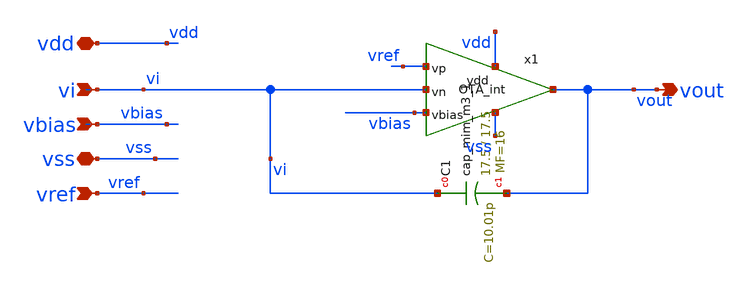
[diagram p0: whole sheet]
** sch_path: xschem/src/integrator/integrator.sch
**.subckt integrator vi vbias vss vdd vout vref
*.ipin vi
*.ipin vbias
*.iopin vss
*.iopin vdd
*.opin vout
*.ipin vref
x1 vdd vref vi vbias vss vout OTA_int
XC1 vi vout sky130_fd_pr__cap_mim_m3_1 W=17.5 L=17.5 MF=16 m=16
**.ends

* expanding   symbol:  src/OTA_int/OTA_int.sym # of pins=6
** sym_path: xschem/src/OTA_int/OTA_int.sym
** sch_path: xschem/src/OTA_int/OTA_int.sch
.subckt OTA_int vdd vp vn vbias vss vout
*.ipin vp
*.ipin vn
*.ipin vbias
*.iopin vss
*.iopin vdd
*.opin vout
XM1 v1 vp vc vc sky130_fd_pr__pfet_01v8_lvt L=1 W=4 nf=1 ad='int((nf+1)/2) * W/nf * 0.29' as='int((nf+2)/2) * W/nf * 0.29'
+ pd='2*int((nf+1)/2) * (W/nf + 0.29)' ps='2*int((nf+2)/2) * (W/nf + 0.29)' nrd='0.29 / W' nrs='0.29 / W'
+ sa=0 sb=0 sd=0 mult=16 m=16
XM2 vf vn vc vc sky130_fd_pr__pfet_01v8_lvt L=1 W=4 nf=1 ad='int((nf+1)/2) * W/nf * 0.29' as='int((nf+2)/2) * W/nf * 0.29'
+ pd='2*int((nf+1)/2) * (W/nf + 0.29)' ps='2*int((nf+2)/2) * (W/nf + 0.29)' nrd='0.29 / W' nrs='0.29 / W'
+ sa=0 sb=0 sd=0 mult=16 m=16
XM3 vc vbias vdd vdd sky130_fd_pr__pfet_01v8_lvt L=1 W=2 nf=2 ad='int((nf+1)/2) * W/nf * 0.29' as='int((nf+2)/2) * W/nf * 0.29'
+ pd='2*int((nf+1)/2) * (W/nf + 0.29)' ps='2*int((nf+2)/2) * (W/nf + 0.29)' nrd='0.29 / W' nrs='0.29 / W'
+ sa=0 sb=0 sd=0 mult=24 m=24
XM4 v1 vf vss vss sky130_fd_pr__nfet_01v8_lvt L=1 W=1 nf=1 ad='int((nf+1)/2) * W/nf * 0.29' as='int((nf+2)/2) * W/nf * 0.29'
+ pd='2*int((nf+1)/2) * (W/nf + 0.29)' ps='2*int((nf+2)/2) * (W/nf + 0.29)' nrd='0.29 / W' nrs='0.29 / W'
+ sa=0 sb=0 sd=0 mult=16 m=16
XM5 vf vf vss vss sky130_fd_pr__nfet_01v8_lvt L=1 W=1 nf=1 ad='int((nf+1)/2) * W/nf * 0.29' as='int((nf+2)/2) * W/nf * 0.29'
+ pd='2*int((nf+1)/2) * (W/nf + 0.29)' ps='2*int((nf+2)/2) * (W/nf + 0.29)' nrd='0.29 / W' nrs='0.29 / W'
+ sa=0 sb=0 sd=0 mult=16 m=16
XM6 vbias vbias vdd vdd sky130_fd_pr__pfet_01v8_lvt L=1 W=2 nf=2 ad='int((nf+1)/2) * W/nf * 0.29' as='int((nf+2)/2) * W/nf * 0.29'
+ pd='2*int((nf+1)/2) * (W/nf + 0.29)' ps='2*int((nf+2)/2) * (W/nf + 0.29)' nrd='0.29 / W' nrs='0.29 / W'
+ sa=0 sb=0 sd=0 mult=24 m=24
XM7 vout vbias vdd vdd sky130_fd_pr__pfet_01v8_lvt L=1 W=2 nf=2 ad='int((nf+1)/2) * W/nf * 0.29' as='int((nf+2)/2) * W/nf * 0.29'
+ pd='2*int((nf+1)/2) * (W/nf + 0.29)' ps='2*int((nf+2)/2) * (W/nf + 0.29)' nrd='0.29 / W' nrs='0.29 / W'
+ sa=0 sb=0 sd=0 mult=48 m=48
XM8 vout v1 vss vss sky130_fd_pr__nfet_01v8_lvt L=1 W=1 nf=1 ad='int((nf+1)/2) * W/nf * 0.29' as='int((nf+2)/2) * W/nf * 0.29'
+ pd='2*int((nf+1)/2) * (W/nf + 0.29)' ps='2*int((nf+2)/2) * (W/nf + 0.29)' nrd='0.29 / W' nrs='0.29 / W'
+ sa=0 sb=0 sd=0 mult=64 m=64
XC1 v2 vout sky130_fd_pr__cap_mim_m3_1 W=14 L=30 MF=1 m=1
XR1 v1 v2 vss sky130_fd_pr__res_xhigh_po L=2.8 mult=1 m=1
XC2 v2 vout sky130_fd_pr__cap_mim_m3_1 W=30 L=14 MF=1 m=1
.ends

.end
